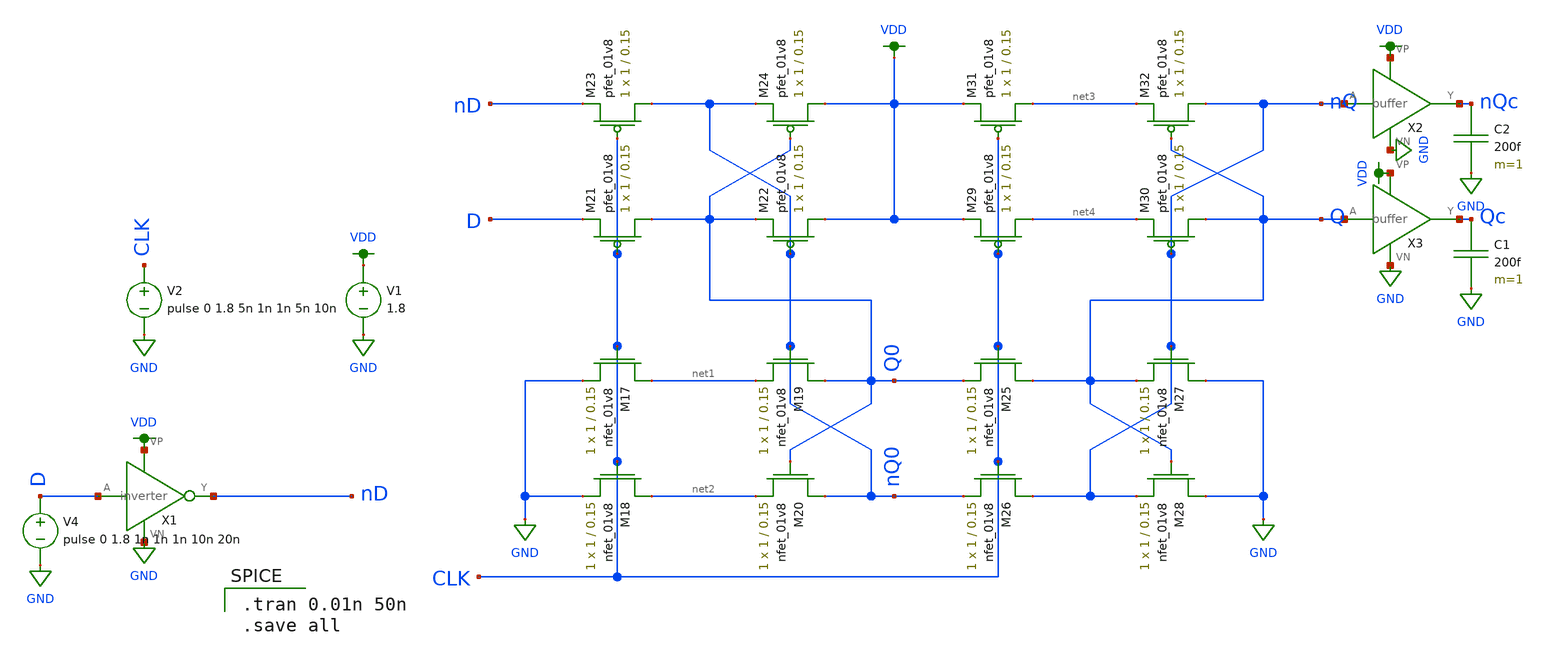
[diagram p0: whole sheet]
** sch_path: mini2/schem/dff_Stest.sch
**.subckt dff_Stest
V1 VDD GND 1.8
V2 CLK GND pulse 0 1.8 5n 1n 1n 5n 10n
V4 D GND pulse 0 1.8 1n 1n 1n 10n 20n
X1 D nD VDD GND inverter
XM17 net1 CLK GND GND sky130_fd_pr__nfet_01v8 L=0.15 W=1 nf=1 ad='int((nf+1)/2) * W/nf * 0.29' as='int((nf+2)/2) * W/nf * 0.29'
+ pd='2*int((nf+1)/2) * (W/nf + 0.29)' ps='2*int((nf+2)/2) * (W/nf + 0.29)' nrd='0.29 / W' nrs='0.29 / W'
+ sa=0 sb=0 sd=0 mult=1 m=1
XM18 net2 CLK GND GND sky130_fd_pr__nfet_01v8 L=0.15 W=1 nf=1 ad='int((nf+1)/2) * W/nf * 0.29' as='int((nf+2)/2) * W/nf * 0.29'
+ pd='2*int((nf+1)/2) * (W/nf + 0.29)' ps='2*int((nf+2)/2) * (W/nf + 0.29)' nrd='0.29 / W' nrs='0.29 / W'
+ sa=0 sb=0 sd=0 mult=1 m=1
XM19 Q0 nQ0 net1 GND sky130_fd_pr__nfet_01v8 L=0.15 W=1 nf=1 ad='int((nf+1)/2) * W/nf * 0.29' as='int((nf+2)/2) * W/nf * 0.29'
+ pd='2*int((nf+1)/2) * (W/nf + 0.29)' ps='2*int((nf+2)/2) * (W/nf + 0.29)' nrd='0.29 / W' nrs='0.29 / W'
+ sa=0 sb=0 sd=0 mult=1 m=1
XM20 nQ0 Q0 net2 GND sky130_fd_pr__nfet_01v8 L=0.15 W=1 nf=1 ad='int((nf+1)/2) * W/nf * 0.29' as='int((nf+2)/2) * W/nf * 0.29'
+ pd='2*int((nf+1)/2) * (W/nf + 0.29)' ps='2*int((nf+2)/2) * (W/nf + 0.29)' nrd='0.29 / W' nrs='0.29 / W'
+ sa=0 sb=0 sd=0 mult=1 m=1
XM21 Q0 CLK D VDD sky130_fd_pr__pfet_01v8 L=0.15 W=1 nf=1 ad='int((nf+1)/2) * W/nf * 0.29' as='int((nf+2)/2) * W/nf * 0.29'
+ pd='2*int((nf+1)/2) * (W/nf + 0.29)' ps='2*int((nf+2)/2) * (W/nf + 0.29)' nrd='0.29 / W' nrs='0.29 / W'
+ sa=0 sb=0 sd=0 mult=1 m=1
XM22 VDD nQ0 Q0 VDD sky130_fd_pr__pfet_01v8 L=0.15 W=1 nf=1 ad='int((nf+1)/2) * W/nf * 0.29' as='int((nf+2)/2) * W/nf * 0.29'
+ pd='2*int((nf+1)/2) * (W/nf + 0.29)' ps='2*int((nf+2)/2) * (W/nf + 0.29)' nrd='0.29 / W' nrs='0.29 / W'
+ sa=0 sb=0 sd=0 mult=1 m=1
XM23 nQ0 CLK nD VDD sky130_fd_pr__pfet_01v8 L=0.15 W=1 nf=1 ad='int((nf+1)/2) * W/nf * 0.29' as='int((nf+2)/2) * W/nf * 0.29'
+ pd='2*int((nf+1)/2) * (W/nf + 0.29)' ps='2*int((nf+2)/2) * (W/nf + 0.29)' nrd='0.29 / W' nrs='0.29 / W'
+ sa=0 sb=0 sd=0 mult=1 m=1
XM24 VDD Q0 nQ0 VDD sky130_fd_pr__pfet_01v8 L=0.15 W=1 nf=1 ad='int((nf+1)/2) * W/nf * 0.29' as='int((nf+2)/2) * W/nf * 0.29'
+ pd='2*int((nf+1)/2) * (W/nf + 0.29)' ps='2*int((nf+2)/2) * (W/nf + 0.29)' nrd='0.29 / W' nrs='0.29 / W'
+ sa=0 sb=0 sd=0 mult=1 m=1
XM25 Q CLK Q0 GND sky130_fd_pr__nfet_01v8 L=0.15 W=1 nf=1 ad='int((nf+1)/2) * W/nf * 0.29' as='int((nf+2)/2) * W/nf * 0.29'
+ pd='2*int((nf+1)/2) * (W/nf + 0.29)' ps='2*int((nf+2)/2) * (W/nf + 0.29)' nrd='0.29 / W' nrs='0.29 / W'
+ sa=0 sb=0 sd=0 mult=1 m=1
XM26 nQ CLK nQ0 GND sky130_fd_pr__nfet_01v8 L=0.15 W=1 nf=1 ad='int((nf+1)/2) * W/nf * 0.29' as='int((nf+2)/2) * W/nf * 0.29'
+ pd='2*int((nf+1)/2) * (W/nf + 0.29)' ps='2*int((nf+2)/2) * (W/nf + 0.29)' nrd='0.29 / W' nrs='0.29 / W'
+ sa=0 sb=0 sd=0 mult=1 m=1
XM27 GND nQ Q GND sky130_fd_pr__nfet_01v8 L=0.15 W=1 nf=1 ad='int((nf+1)/2) * W/nf * 0.29' as='int((nf+2)/2) * W/nf * 0.29'
+ pd='2*int((nf+1)/2) * (W/nf + 0.29)' ps='2*int((nf+2)/2) * (W/nf + 0.29)' nrd='0.29 / W' nrs='0.29 / W'
+ sa=0 sb=0 sd=0 mult=1 m=1
XM28 GND Q nQ GND sky130_fd_pr__nfet_01v8 L=0.15 W=1 nf=1 ad='int((nf+1)/2) * W/nf * 0.29' as='int((nf+2)/2) * W/nf * 0.29'
+ pd='2*int((nf+1)/2) * (W/nf + 0.29)' ps='2*int((nf+2)/2) * (W/nf + 0.29)' nrd='0.29 / W' nrs='0.29 / W'
+ sa=0 sb=0 sd=0 mult=1 m=1
XM29 net4 CLK VDD VDD sky130_fd_pr__pfet_01v8 L=0.15 W=1 nf=1 ad='int((nf+1)/2) * W/nf * 0.29' as='int((nf+2)/2) * W/nf * 0.29'
+ pd='2*int((nf+1)/2) * (W/nf + 0.29)' ps='2*int((nf+2)/2) * (W/nf + 0.29)' nrd='0.29 / W' nrs='0.29 / W'
+ sa=0 sb=0 sd=0 mult=1 m=1
XM30 Q nQ net4 VDD sky130_fd_pr__pfet_01v8 L=0.15 W=1 nf=1 ad='int((nf+1)/2) * W/nf * 0.29' as='int((nf+2)/2) * W/nf * 0.29'
+ pd='2*int((nf+1)/2) * (W/nf + 0.29)' ps='2*int((nf+2)/2) * (W/nf + 0.29)' nrd='0.29 / W' nrs='0.29 / W'
+ sa=0 sb=0 sd=0 mult=1 m=1
XM31 net3 CLK VDD VDD sky130_fd_pr__pfet_01v8 L=0.15 W=1 nf=1 ad='int((nf+1)/2) * W/nf * 0.29' as='int((nf+2)/2) * W/nf * 0.29'
+ pd='2*int((nf+1)/2) * (W/nf + 0.29)' ps='2*int((nf+2)/2) * (W/nf + 0.29)' nrd='0.29 / W' nrs='0.29 / W'
+ sa=0 sb=0 sd=0 mult=1 m=1
XM32 nQ Q net3 VDD sky130_fd_pr__pfet_01v8 L=0.15 W=1 nf=1 ad='int((nf+1)/2) * W/nf * 0.29' as='int((nf+2)/2) * W/nf * 0.29'
+ pd='2*int((nf+1)/2) * (W/nf + 0.29)' ps='2*int((nf+2)/2) * (W/nf + 0.29)' nrd='0.29 / W' nrs='0.29 / W'
+ sa=0 sb=0 sd=0 mult=1 m=1
C1 Qc GND 200f m=1
C2 nQc GND 200f m=1
X2 nQ nQc VDD GND buffer
X3 Q Qc VDD GND buffer
**** begin user architecture code

.option wnflag=1
.lib ~/skywater/skywater-pdk/libraries/sky130_fd_pr_ngspice/latest/models/sky130.lib.spice tt


.tran 0.01n 50n
.save all

**** end user architecture code
**.ends
.GLOBAL VDD
.GLOBAL GND
.end
